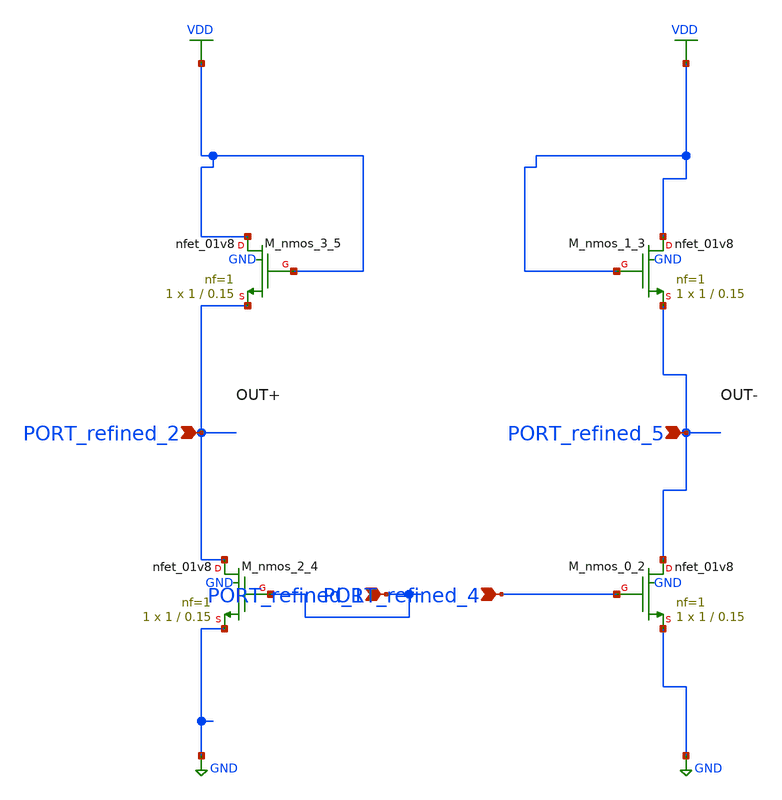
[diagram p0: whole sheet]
** sch_path: schematics/SchemGen/no_doi_05_001_crop2.sch
**.subckt no_doi_05_001_crop2 PORT_refined_2 PORT_refined_5 PORT_refined_4 PORT_refined_1
*.ipin PORT_refined_2
*.ipin PORT_refined_5
*.ipin PORT_refined_4
*.ipin PORT_refined_1
XM_nmos_0_2 PORT_refined_5 PORT_refined_4 GND GND sky130_fd_pr__nfet_01v8 L=0.15 W=1 nf=1 ad='int((1 + 1)/2) * 1 / 1 * 0.29'
+ as='int((1 + 2)/2) * 1 / 1 * 0.29' pd='2*int((1 + 1)/2) * (1 / 1 + 0.29)' ps='2*int((1 + 2)/2) * (1 / 1 + 0.29)'
+ nrd='0.29 / 1 ' nrs='0.29 / 1 ' sa=0 sb=0 sd=0 mult=1 m=1
XM_nmos_1_3 VDD VDD PORT_refined_5 GND sky130_fd_pr__nfet_01v8 L=0.15 W=1 nf=1 ad='int((1 + 1)/2) * 1 / 1 * 0.29'
+ as='int((1 + 2)/2) * 1 / 1 * 0.29' pd='2*int((1 + 1)/2) * (1 / 1 + 0.29)' ps='2*int((1 + 2)/2) * (1 / 1 + 0.29)'
+ nrd='0.29 / 1 ' nrs='0.29 / 1 ' sa=0 sb=0 sd=0 mult=1 m=1
XM_nmos_2_4 PORT_refined_2 PORT_refined_1 GND GND sky130_fd_pr__nfet_01v8 L=0.15 W=1 nf=1 ad='int((1 + 1)/2) * 1 / 1 * 0.29'
+ as='int((1 + 2)/2) * 1 / 1 * 0.29' pd='2*int((1 + 1)/2) * (1 / 1 + 0.29)' ps='2*int((1 + 2)/2) * (1 / 1 + 0.29)'
+ nrd='0.29 / 1 ' nrs='0.29 / 1 ' sa=0 sb=0 sd=0 mult=1 m=1
XM_nmos_3_5 VDD VDD PORT_refined_2 GND sky130_fd_pr__nfet_01v8 L=0.15 W=1 nf=1 ad='int((1 + 1)/2) * 1 / 1 * 0.29'
+ as='int((1 + 2)/2) * 1 / 1 * 0.29' pd='2*int((1 + 1)/2) * (1 / 1 + 0.29)' ps='2*int((1 + 2)/2) * (1 / 1 + 0.29)'
+ nrd='0.29 / 1 ' nrs='0.29 / 1 ' sa=0 sb=0 sd=0 mult=1 m=1
**.ends
.GLOBAL GND
.GLOBAL VDD
.end
